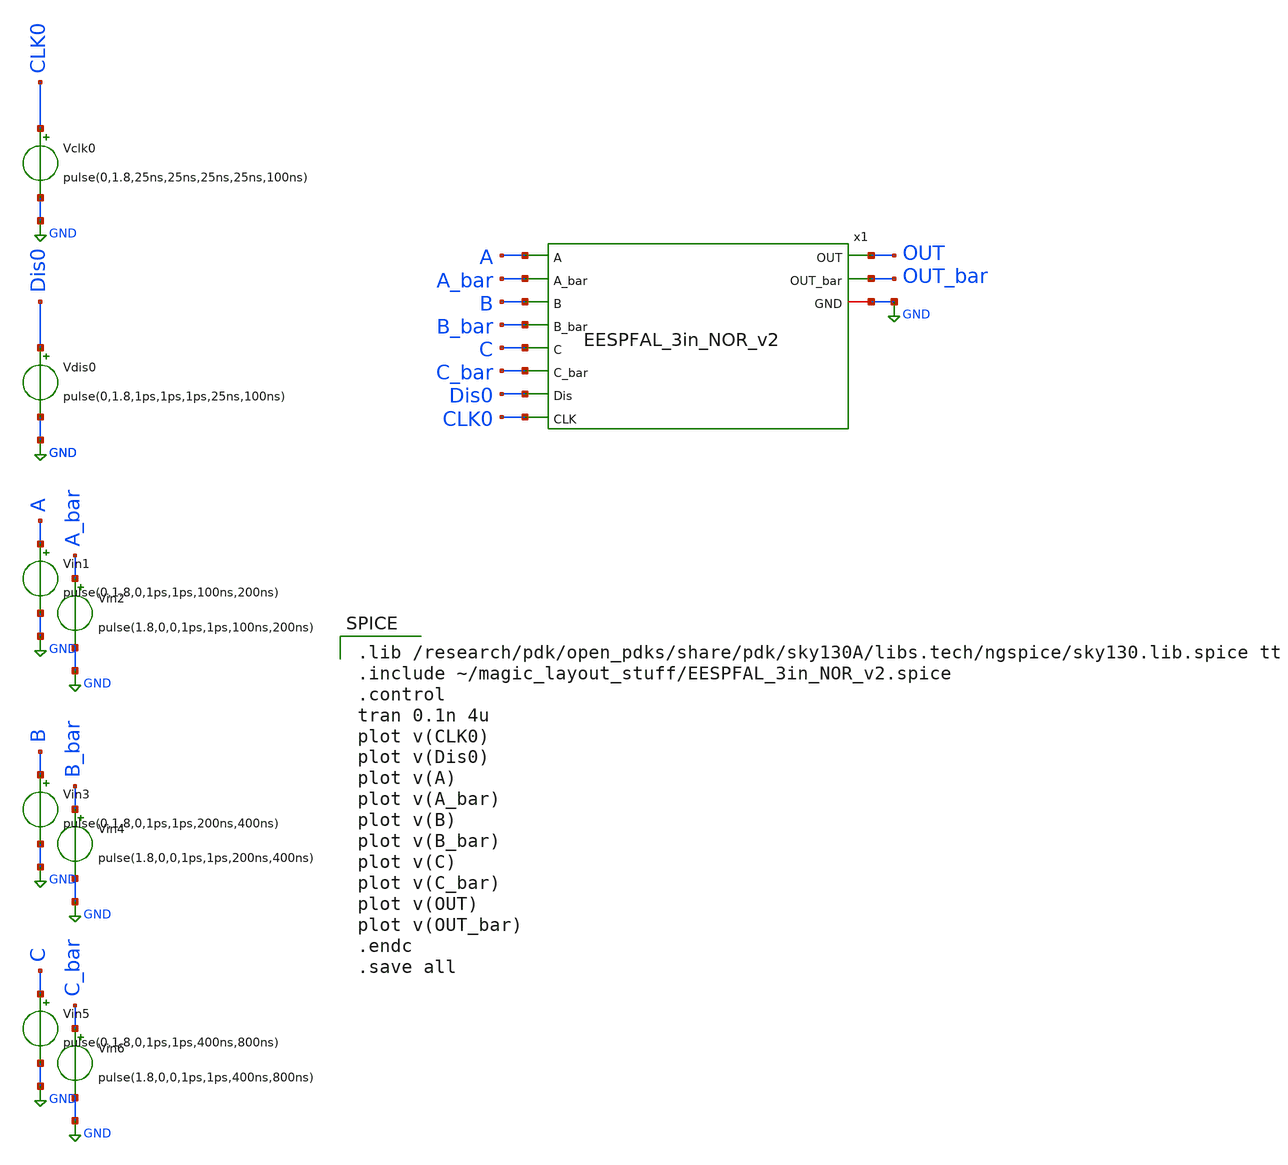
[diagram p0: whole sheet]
** sch_path: skywater_stuff/EESPFAL_3in_NOR_sim.sch
**.subckt EESPFAL_3in_NOR_sim
Vclk0 CLK0 GND pulse(0,1.8,25ns,25ns,25ns,25ns,100ns)
Vin1 A GND pulse(0,1.8,0,1ps,1ps,100ns,200ns)
Vin2 A_bar GND pulse(1.8,0,0,1ps,1ps,100ns,200ns)
Vdis0 Dis0 GND pulse(0,1.8,1ps,1ps,1ps,25ns,100ns)
Vin3 B GND pulse(0,1.8,0,1ps,1ps,200ns,400ns)
Vin4 B_bar GND pulse(1.8,0,0,1ps,1ps,200ns,400ns)
Vin5 C GND pulse(0,1.8,0,1ps,1ps,400ns,800ns)
Vin6 C_bar GND pulse(1.8,0,0,1ps,1ps,400ns,800ns)
x1 A A_bar B B_bar C C_bar OUT OUT_bar Dis0 GND CLK0 EESPFAL_3in_NOR_v2
**** begin user architecture code

.lib /research/pdk/open_pdks/share/pdk/sky130A/libs.tech/ngspice/sky130.lib.spice tt
.include ~/magic_layout_stuff/EESPFAL_3in_NOR_v2.spice
.control
tran 0.1n 4u
plot v(CLK0)
plot v(Dis0)
plot v(A)
plot v(A_bar)
plot v(B)
plot v(B_bar)
plot v(C)
plot v(C_bar)
plot v(OUT)
plot v(OUT_bar)
.endc
.save all

**** end user architecture code
**.ends
.GLOBAL GND
.end
